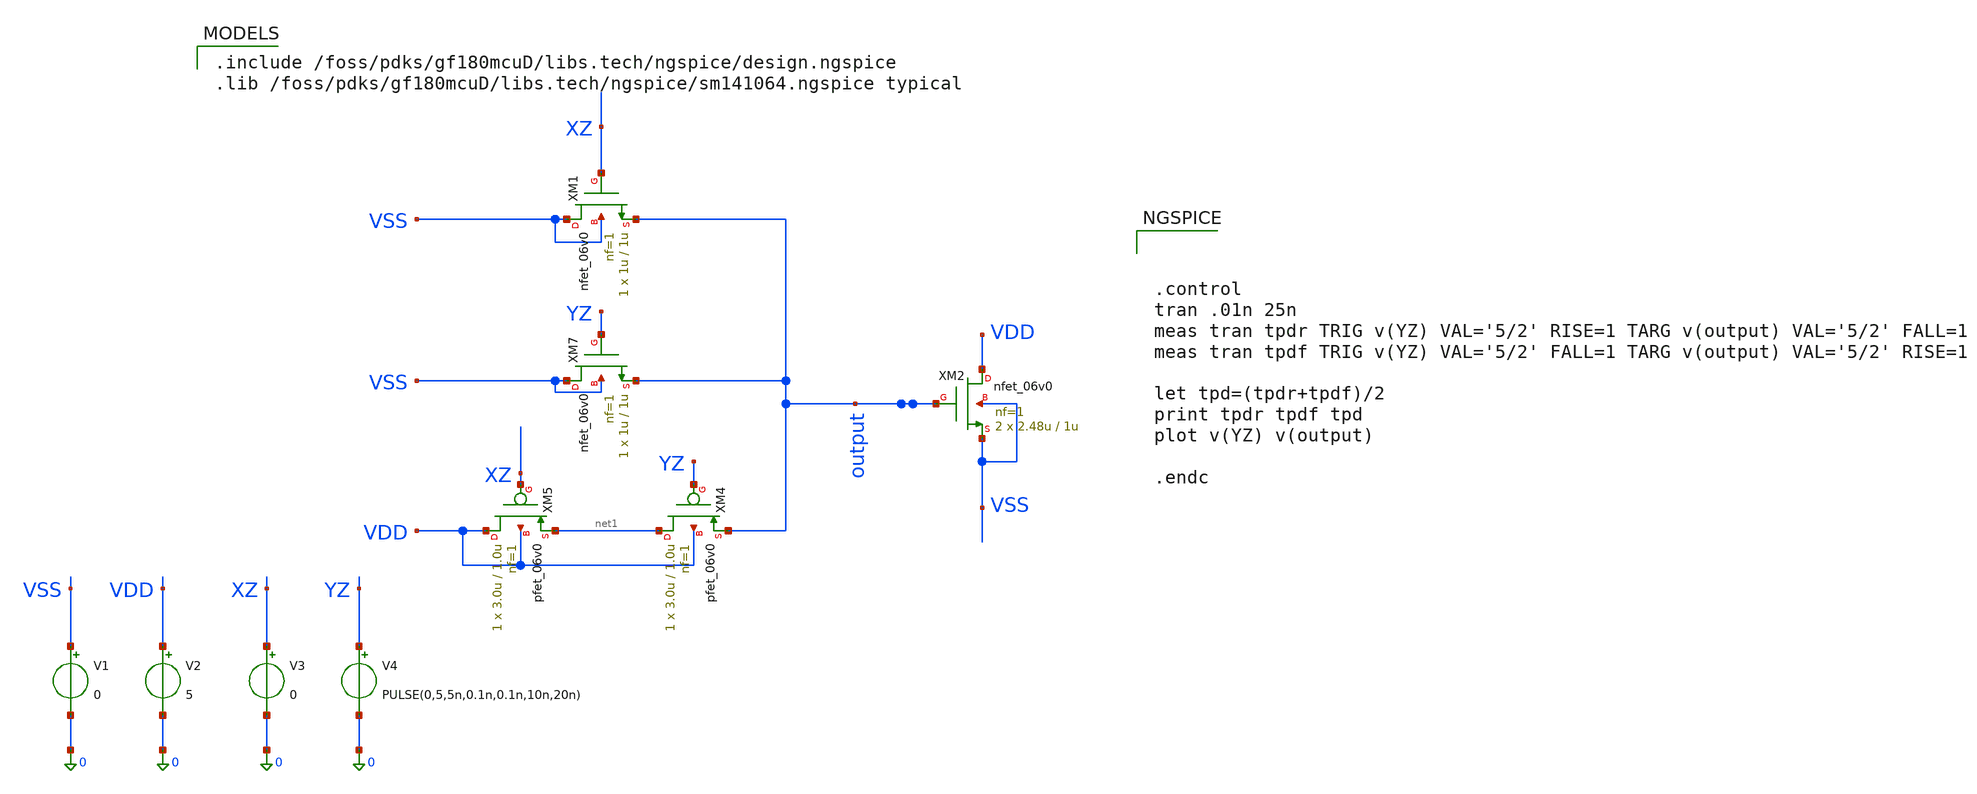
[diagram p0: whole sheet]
** sch_path: activities/opamp3AKAM/zDelayTB2.sch
**.subckt zDelayTB2
XM4 net1 YZ output VDD pfet_06v0 L=1.0u W=3.0u nf=1 ad='int((nf+1)/2) * W/nf * 0.18u' as='int((nf+2)/2) * W/nf * 0.18u'
+ pd='2*int((nf+1)/2) * (W/nf + 0.18u)' ps='2*int((nf+2)/2) * (W/nf + 0.18u)' nrd='0.18u / W' nrs='0.18u / W'
+ sa=0 sb=0 sd=0 m=1
XM5 VDD XZ net1 VDD pfet_06v0 L=1.0u W=3.0u nf=1 ad='int((nf+1)/2) * W/nf * 0.18u' as='int((nf+2)/2) * W/nf * 0.18u'
+ pd='2*int((nf+1)/2) * (W/nf + 0.18u)' ps='2*int((nf+2)/2) * (W/nf + 0.18u)' nrd='0.18u / W' nrs='0.18u / W'
+ sa=0 sb=0 sd=0 m=1
XM7 VSS YZ output VSS nfet_06v0 L=1u W=1u nf=1 ad='int((nf+1)/2) * W/nf * 0.18u' as='int((nf+2)/2) * W/nf * 0.18u'
+ pd='2*int((nf+1)/2) * (W/nf + 0.18u)' ps='2*int((nf+2)/2) * (W/nf + 0.18u)' nrd='0.18u / W' nrs='0.18u / W'
+ sa=0 sb=0 sd=0 m=1
XM1 VSS XZ output VSS nfet_06v0 L=1u W=1u nf=1 ad='int((nf+1)/2) * W/nf * 0.18u' as='int((nf+2)/2) * W/nf * 0.18u'
+ pd='2*int((nf+1)/2) * (W/nf + 0.18u)' ps='2*int((nf+2)/2) * (W/nf + 0.18u)' nrd='0.18u / W' nrs='0.18u / W'
+ sa=0 sb=0 sd=0 m=1
V1 VSS 0 0
V2 VDD 0 5
V3 XZ 0 0
V4 YZ 0 PULSE(0,5,5n,0.1n,0.1n,10n,20n)
XM2 VDD output VSS VSS nfet_06v0 L=1u W=2.48u nf=1 ad='int((nf+1)/2) * W/nf * 0.18u' as='int((nf+2)/2) * W/nf * 0.18u'
+ pd='2*int((nf+1)/2) * (W/nf + 0.18u)' ps='2*int((nf+2)/2) * (W/nf + 0.18u)' nrd='0.18u / W' nrs='0.18u / W'
+ sa=0 sb=0 sd=0 m=2
**** begin user architecture code

.include /foss/pdks/gf180mcuD/libs.tech/ngspice/design.ngspice
.lib /foss/pdks/gf180mcuD/libs.tech/ngspice/sm141064.ngspice typical




.control
tran .01n 25n
meas tran tpdr TRIG v(YZ) VAL='5/2' RISE=1 TARG v(output) VAL='5/2' FALL=1
meas tran tpdf TRIG v(YZ) VAL='5/2' FALL=1 TARG v(output) VAL='5/2' RISE=1

let tpd=(tpdr+tpdf)/2
print tpdr tpdf tpd
plot v(YZ) v(output)

.endc


**** end user architecture code
**.ends
.end
